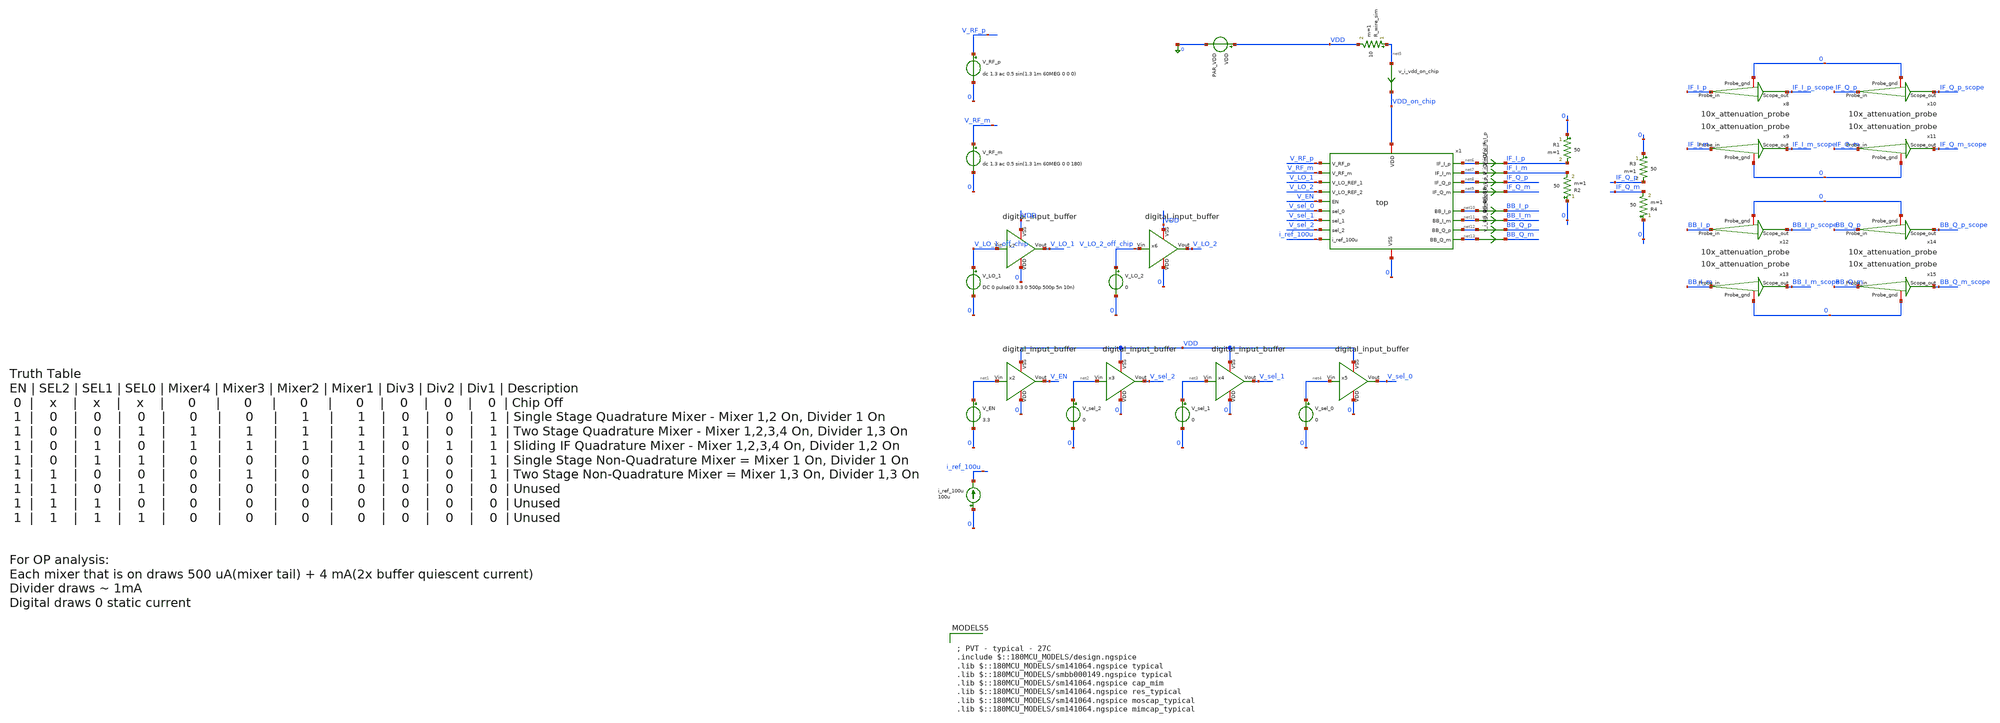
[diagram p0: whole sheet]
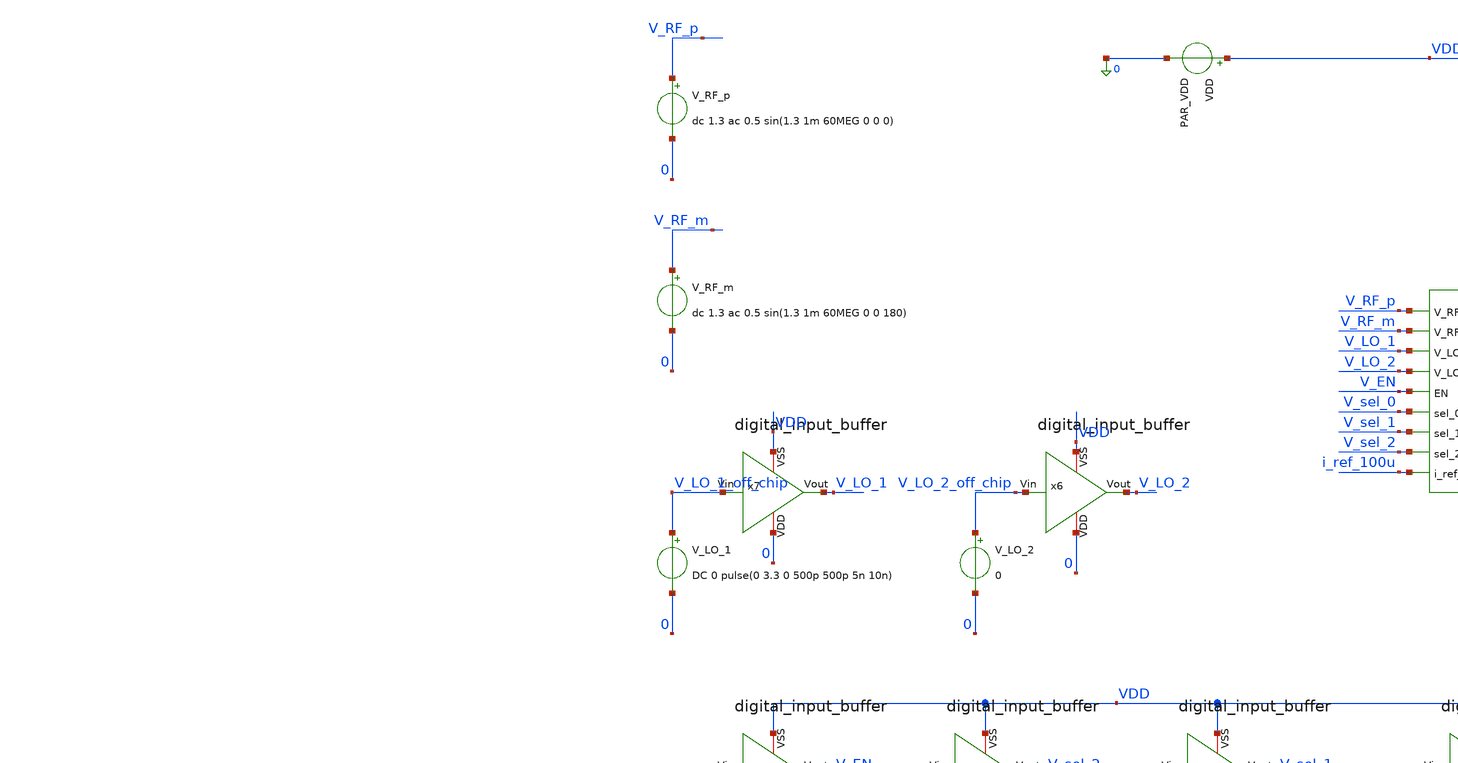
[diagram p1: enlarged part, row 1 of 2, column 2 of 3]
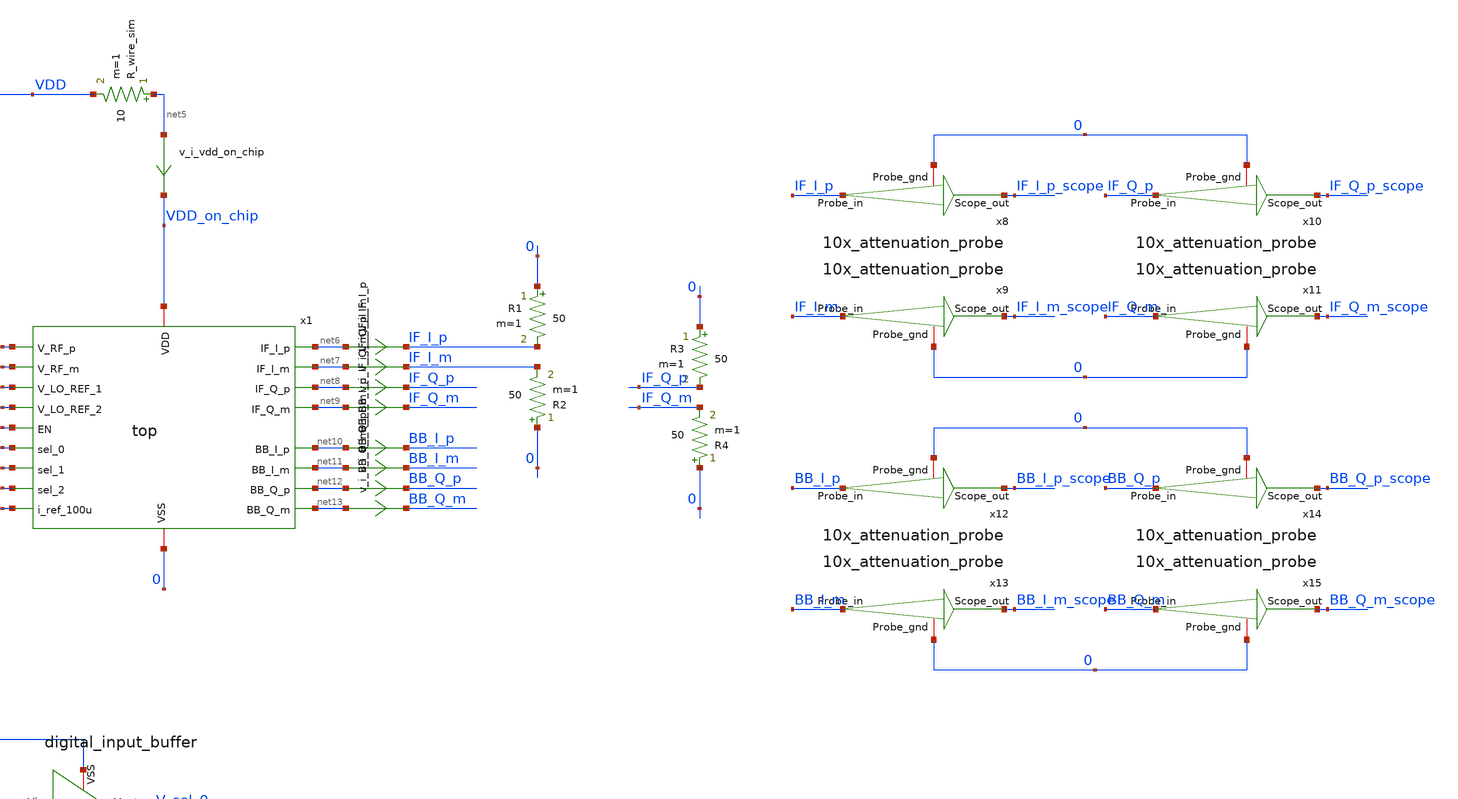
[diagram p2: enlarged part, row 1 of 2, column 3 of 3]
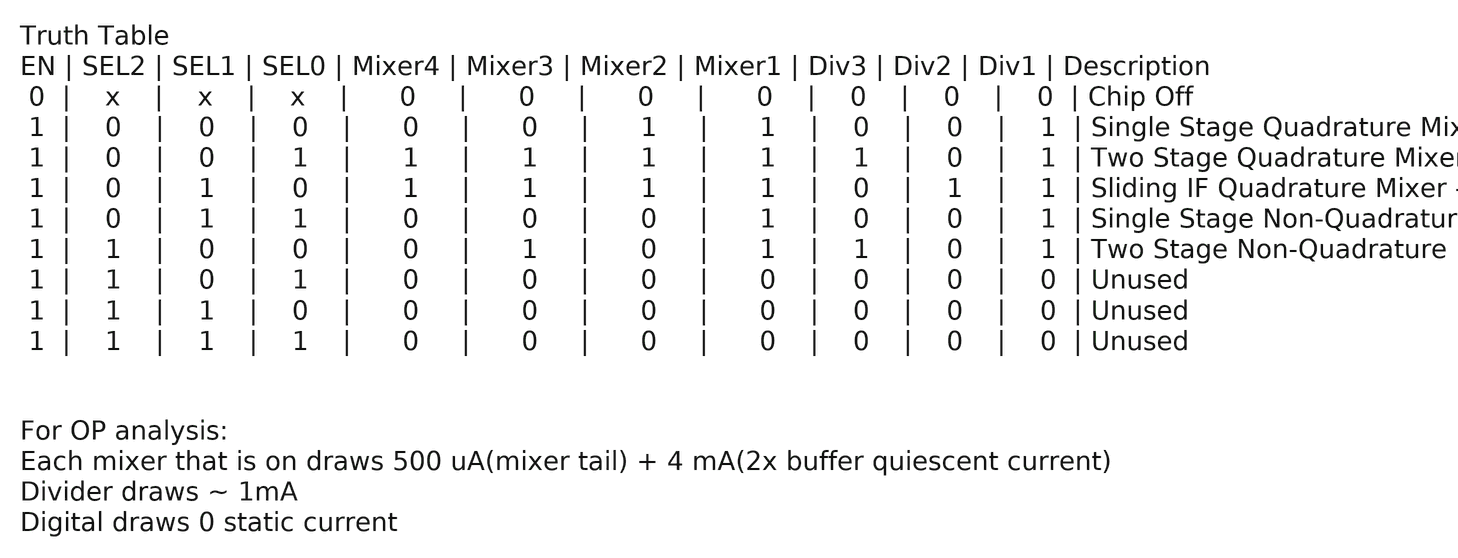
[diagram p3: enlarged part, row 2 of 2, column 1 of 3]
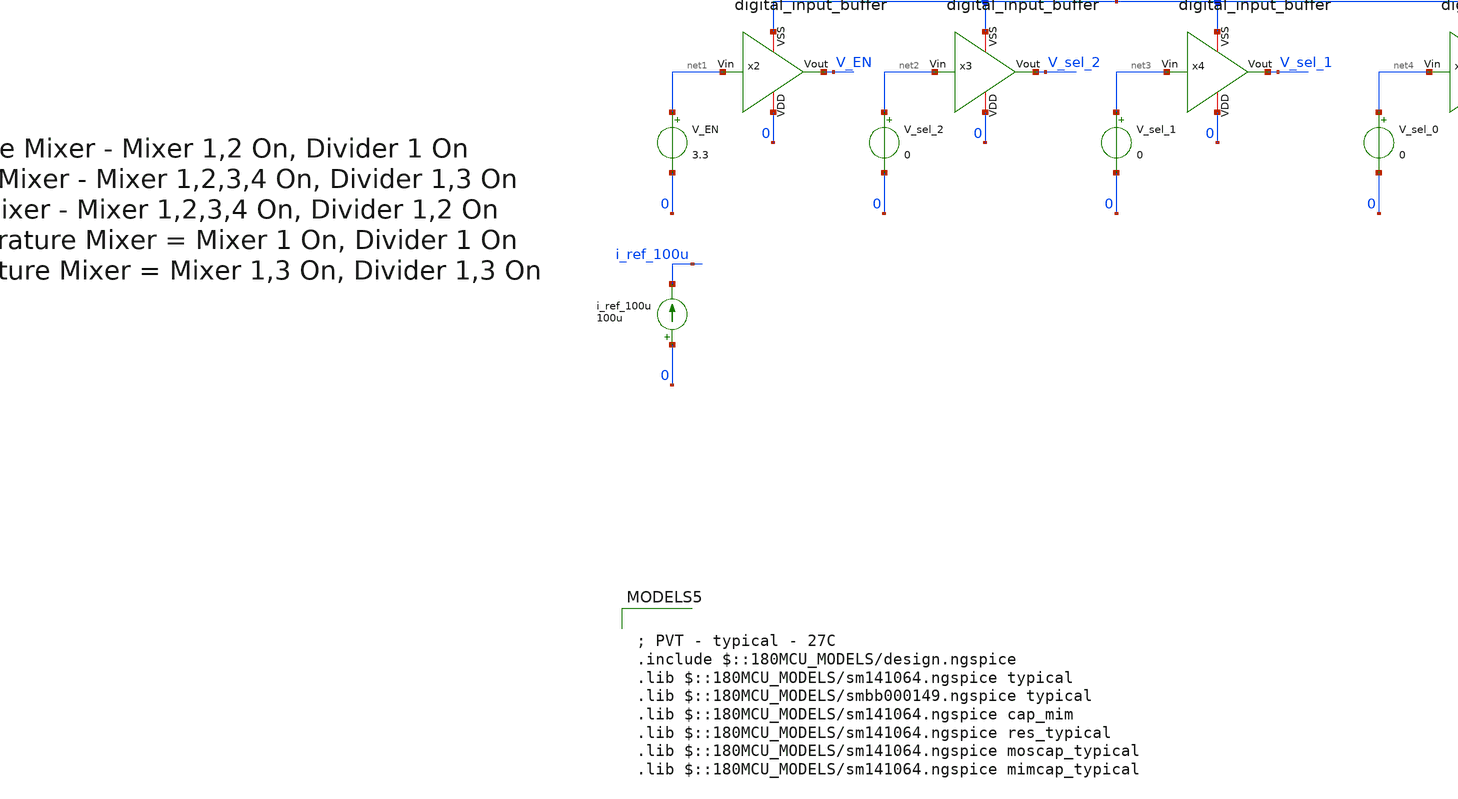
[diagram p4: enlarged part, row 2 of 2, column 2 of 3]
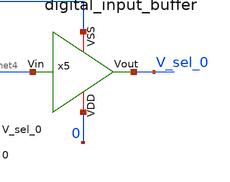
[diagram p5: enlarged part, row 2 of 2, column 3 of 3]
** sch_path: designs/top_level/testbench/tb_top.sch
**.subckt tb_top
x1 V_RF_p VDD_on_chip V_RF_m 0 V_LO_1 net6 net7 V_LO_2 net8 V_EN net9 V_sel_0 V_sel_1 net10 V_sel_2
+ net11 net12 i_ref_100u net13 top
VDD VDD 0 PAR_VDD
V_RF_p V_RF_p 0 dc 1.3 ac 0.5 sin(1.3 1m 60MEG 0 0 0)
R_wire_sim net5 VDD 10 m=1
V_RF_m V_RF_m 0 dc 1.3 ac 0.5 sin(1.3 1m 60MEG 0 0 180)
V_LO_1 V_LO_1_off_chip 0 DC 0 pulse(0 3.3 0 500p 500p 5n 10n)
V_LO_2 V_LO_2_off_chip 0 0
V_EN net1 0 3.3
V_sel_2 net2 0 0
V_sel_1 net3 0 0
V_sel_0 net4 0 0
i_ref_100u 0 i_ref_100u 100u
x2 VDD net1 V_EN 0 digital_input_buffer
x3 VDD net2 V_sel_2 0 digital_input_buffer
x4 VDD net3 V_sel_1 0 digital_input_buffer
x5 VDD net4 V_sel_0 0 digital_input_buffer
x6 VDD V_LO_2_off_chip V_LO_2 0 digital_input_buffer
x7 VDD V_LO_1_off_chip V_LO_1 0 digital_input_buffer
x8 IF_I_p IF_I_p_scope 0 10x_attenuation_probe
x9 IF_I_m IF_I_m_scope 0 10x_attenuation_probe
x10 IF_Q_p IF_Q_p_scope 0 10x_attenuation_probe
x11 IF_Q_m IF_Q_m_scope 0 10x_attenuation_probe
x12 BB_I_p BB_I_p_scope 0 10x_attenuation_probe
x13 BB_I_m BB_I_m_scope 0 10x_attenuation_probe
x14 BB_Q_p BB_Q_p_scope 0 10x_attenuation_probe
x15 BB_Q_m BB_Q_m_scope 0 10x_attenuation_probe
v_i_vdd_on_chip net5 VDD_on_chip 0
.save i(v_i_vdd_on_chip)
v_i_IF_I_p net6 IF_I_p 0
.save i(v_i_if_i_p)
v_i_IF_I_m net7 IF_I_m 0
.save i(v_i_if_i_m)
v_i_IF_Q_p net8 IF_Q_p 0
.save i(v_i_if_q_p)
v_i_IF_Q_m net9 IF_Q_m 0
.save i(v_i_if_q_m)
v_i_BB_I_p net10 BB_I_p 0
.save i(v_i_bb_i_p)
v_i_BB_I_m net11 BB_I_m 0
.save i(v_i_bb_i_m)
v_i_BB_Q_p net12 BB_Q_p 0
.save i(v_i_bb_q_p)
v_i_BB_Q_m net13 BB_Q_m 0
.save i(v_i_bb_q_m)
R1 0 IF_I_p 50 m=1
R2 0 IF_I_m 50 m=1
R3 0 IF_Q_p 50 m=1
R4 0 IF_Q_m 50 m=1
**** begin user architecture code

; PVT - typical - 27C
.include $::180MCU_MODELS/design.ngspice
.lib $::180MCU_MODELS/sm141064.ngspice typical
.lib $::180MCU_MODELS/smbb000149.ngspice typical
.lib $::180MCU_MODELS/sm141064.ngspice cap_mim
.lib $::180MCU_MODELS/sm141064.ngspice res_typical
.lib $::180MCU_MODELS/sm141064.ngspice moscap_typical
.lib $::180MCU_MODELS/sm141064.ngspice mimcap_typical



** PARAMS

.PARAM PAR_VDD=3.3

.control
destroy all
save all

write tb_top.raw

tran .1n 2u

let vrf = V_rf_p - V_rf_m
let vif_i = if_i_p - if_i_m
let vif_q = if_q_p - if_q_m
let vbb_i = bb_i_p - bb_i_m
let vbb_q = bb_q_p - bb_q_m

plot vrf   ;input signal
plot vif_i ;output in phase
plot vif_q ;output q phase
plot v_lo_1 v_lo_1_off_chip x1.div_1_lo_i_p x1.div_1_lo_i_m ;clock divider

meas tran i_vdd avg i(v_i_vdd_on_chip) from=.3u to=2u ;average vdd current from .3us to 2us
meas tran i_mix_1 avg i(v.x1.v_i_mix_1) from=.3u to=2u ;average vdd current from .3us to 2us
meas tran i_mix_2 avg i(v.x1.v_i_mix_2) from=.3u to=2u ;average vdd current from .3us to 2us
meas tran i_buf_mix_1_p avg i(v.x1.v_i_buf_mix_1_p) from=.3u to=2u ;average vdd current from .3us to
+ 2us
meas tran i_buf_mix_1_m avg i(v.x1.v_i_buf_mix_1_m) from=.3u to=2u ;average vdd current from .3us to
+ 2us
meas tran i_buf_mix_2_p avg i(v.x1.v_i_buf_mix_2_p) from=.3u to=2u ;average vdd current from .3us to
+ 2us
meas tran i_buf_mix_2_m avg i(v.x1.v_i_buf_mix_2_m) from=.3u to=2u ;average vdd current from .3us to
+ 2us

plot i(v_i_vdd_on_chip) i(v.x1.v_i_mix_1) i(v.x1.v_i_mix_2) i(v.x1.v_i_buf_mix_1_p)
+ i(v.x1.v_i_buf_mix_1_m) i(v.x1.v_i_buf_mix_2_p) i(v.x1.v_i_buf_mix_2_m); current in active blocks

print i_vdd
print i_mix_1
print i_mix_2
print i_buf_mix_1_p
print i_buf_mix_1_m
print i_buf_mix_2_p
print i_buf_mix_2_m

let i_blocks = i_mix_1+i_mix_2+i_buf_mix_1_p+i_buf_mix_1_m+i_buf_mix_2_p+i_buf_mix_2_m
print i_vdd-i_blocks

linearize vrf vif_i vif_q v_lo_1 v_lo_1_off_chip x1.div_1_lo_i_p x1.div_1_lo_i_m
fft vrf vif_i vif_q v_lo_1 v_lo_1_off_chip x1.div_1_lo_i_p x1.div_1_lo_i_m

plot db(vrf) xlimit 1 200Meg; input signal
plot db(vif_i) xlimit 1 200MEG;
plot db(vif_q) xlimit 1 200MEG;
plot db(v_lo_1_off_chip) db(x1.div_1_lo_i_p) xlimit 1 200MEG;

.endc


**** end user architecture code
**.ends
.end
